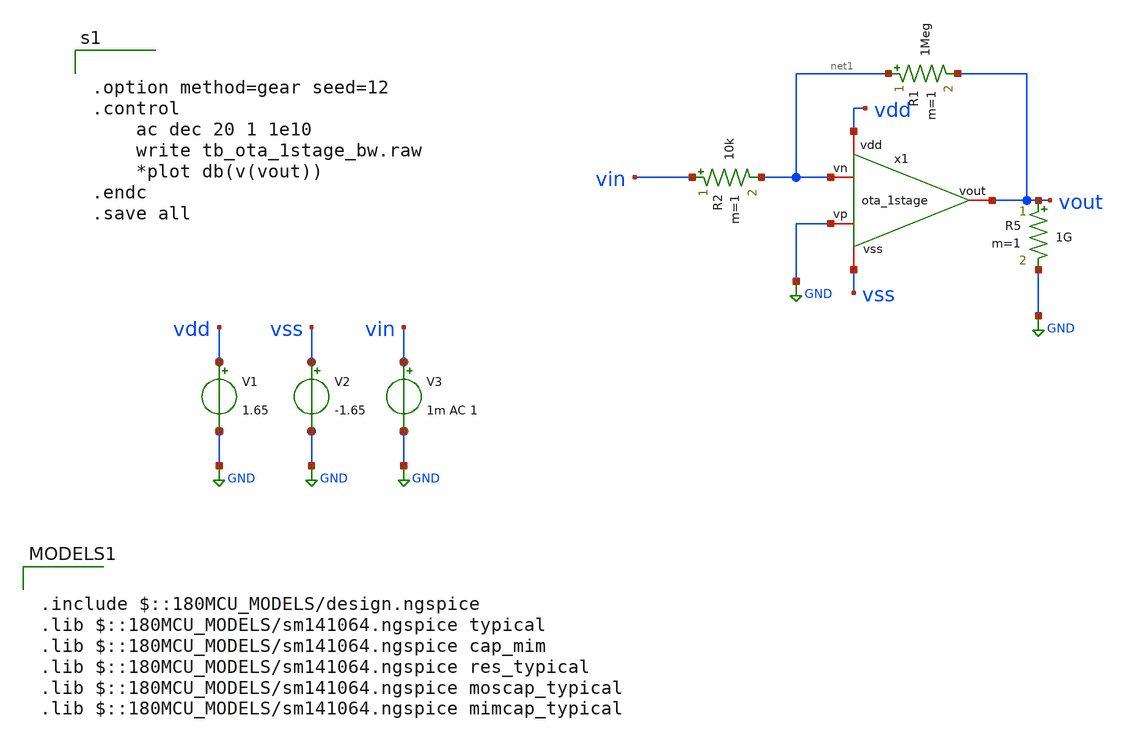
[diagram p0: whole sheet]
** sch_path: designs/libs/core_LIF_comp/tb_ota_1stage/tb_ota_1stage_bw.sch
**.subckt tb_ota_1stage_bw
V1 vdd GND 1.65
V3 vin GND 1m AC 1
R1 net1 vout 1Meg m=1
R2 vin net1 10k m=1
V2 vss GND -1.65
R5 vout GND 1G m=1
x1 vdd vout GND net1 vss ota_1stage
**** begin user architecture code


.option method=gear seed=12
.control
	ac dec 20 1 1e10
	write tb_ota_1stage_bw.raw
	*plot db(v(vout))
.endc
.save all



.include $::180MCU_MODELS/design.ngspice
.lib $::180MCU_MODELS/sm141064.ngspice typical
.lib $::180MCU_MODELS/sm141064.ngspice cap_mim
.lib $::180MCU_MODELS/sm141064.ngspice res_typical
.lib $::180MCU_MODELS/sm141064.ngspice moscap_typical
.lib $::180MCU_MODELS/sm141064.ngspice mimcap_typical

**** end user architecture code
**.ends

* expanding   symbol:  designs/libs/core_LIF_comp/core_ota_1stage/ota_1stage.sym # of pins=5
** sym_path: designs/libs/core_LIF_comp/core_ota_1stage/ota_1stage.sym
** sch_path: designs/libs/core_LIF_comp/core_ota_1stage/ota_1stage.sch
.subckt ota_1stage vdd vout vp vn vss
*.iopin vdd
*.iopin vss
*.iopin vp
*.iopin vn
*.iopin vout
XM1 net1 net1 vdd vdd pfet_03v3 L=0.28u W=0.84u nf=1 ad='int((nf+1)/2) * W/nf * 0.18u' as='int((nf+2)/2) * W/nf * 0.18u'
+ pd='2*int((nf+1)/2) * (W/nf + 0.18u)' ps='2*int((nf+2)/2) * (W/nf + 0.18u)' nrd='0.18u / W' nrs='0.18u / W'
+ sa=0 sb=0 sd=0 m=1
XM2 net1 vp net2 vss nfet_03v3 L=0.28u W=3.08u nf=1 ad='int((nf+1)/2) * W/nf * 0.18u' as='int((nf+2)/2) * W/nf * 0.18u'
+ pd='2*int((nf+1)/2) * (W/nf + 0.18u)' ps='2*int((nf+2)/2) * (W/nf + 0.18u)' nrd='0.18u / W' nrs='0.18u / W'
+ sa=0 sb=0 sd=0 m=1
XM4 vout net1 vdd vdd pfet_03v3 L=0.28u W=0.84u nf=1 ad='int((nf+1)/2) * W/nf * 0.18u' as='int((nf+2)/2) * W/nf * 0.18u'
+ pd='2*int((nf+1)/2) * (W/nf + 0.18u)' ps='2*int((nf+2)/2) * (W/nf + 0.18u)' nrd='0.18u / W' nrs='0.18u / W'
+ sa=0 sb=0 sd=0 m=1
XM3 vout vn net2 vss nfet_03v3 L=0.28u W=3.08u nf=1 ad='int((nf+1)/2) * W/nf * 0.18u' as='int((nf+2)/2) * W/nf * 0.18u'
+ pd='2*int((nf+1)/2) * (W/nf + 0.18u)' ps='2*int((nf+2)/2) * (W/nf + 0.18u)' nrd='0.18u / W' nrs='0.18u / W'
+ sa=0 sb=0 sd=0 m=1
XM5 net2 net3 vss vss nfet_03v3 L=0.28u W=0.84u nf=1 ad='int((nf+1)/2) * W/nf * 0.18u' as='int((nf+2)/2) * W/nf * 0.18u'
+ pd='2*int((nf+1)/2) * (W/nf + 0.18u)' ps='2*int((nf+2)/2) * (W/nf + 0.18u)' nrd='0.18u / W' nrs='0.18u / W'
+ sa=0 sb=0 sd=0 m=1
XM6 net3 net3 vss vss nfet_03v3 L=0.28u W=0.84u nf=1 ad='int((nf+1)/2) * W/nf * 0.18u' as='int((nf+2)/2) * W/nf * 0.18u'
+ pd='2*int((nf+1)/2) * (W/nf + 0.18u)' ps='2*int((nf+2)/2) * (W/nf + 0.18u)' nrd='0.18u / W' nrs='0.18u / W'
+ sa=0 sb=0 sd=0 m=1
XM7 vdd vdd net3 vss nfet_03v3 L=8.54u W=0.28u nf=1 ad='int((nf+1)/2) * W/nf * 0.18u' as='int((nf+2)/2) * W/nf * 0.18u'
+ pd='2*int((nf+1)/2) * (W/nf + 0.18u)' ps='2*int((nf+2)/2) * (W/nf + 0.18u)' nrd='0.18u / W' nrs='0.18u / W'
+ sa=0 sb=0 sd=0 m=1
.ends

.GLOBAL GND
.end
